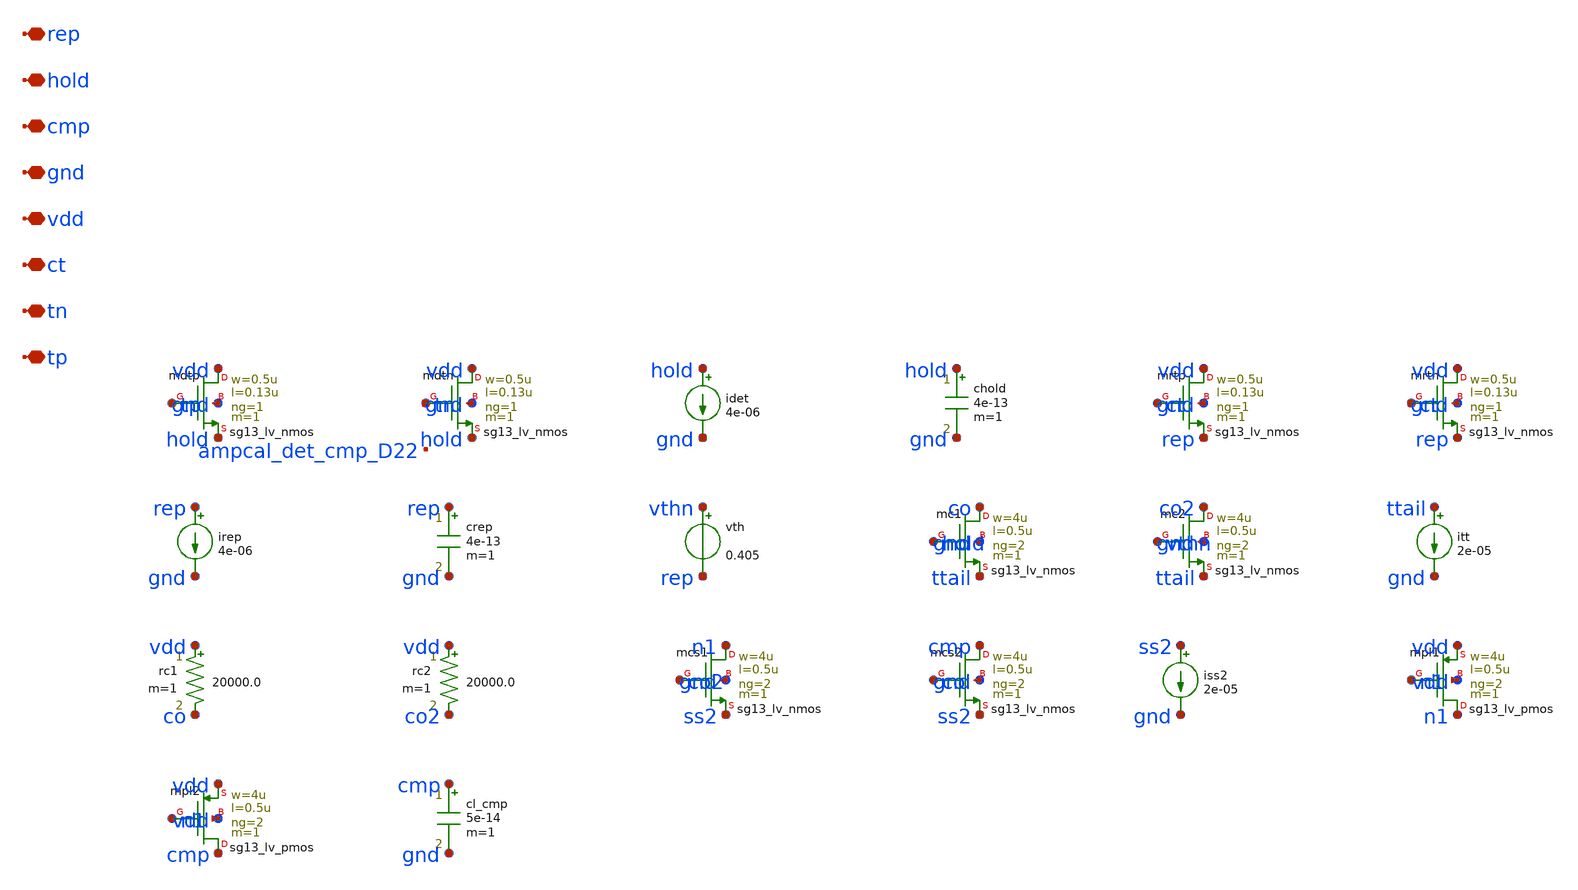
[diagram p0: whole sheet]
** sch_path: analog/vco/sch/ampcal_det.sch
**.subckt ampcal_det tp tn ct vdd gnd cmp hold rep
*.iopin tp
*.iopin tn
*.iopin ct
*.iopin vdd
*.iopin gnd
*.iopin cmp
*.iopin hold
*.iopin rep
Xmdtp vdd tp hold gnd sg13_lv_nmos w=0.5u l=0.13u ng=1 m=1 mm_ok=1
Xmdtn vdd tn hold gnd sg13_lv_nmos w=0.5u l=0.13u ng=1 m=1 mm_ok=1
idet hold gnd 4e-06
chold hold gnd 4e-13 m=1
Xmrtp vdd ct rep gnd sg13_lv_nmos w=0.5u l=0.13u ng=1 m=1 mm_ok=1
Xmrtn vdd ct rep gnd sg13_lv_nmos w=0.5u l=0.13u ng=1 m=1 mm_ok=1
irep rep gnd 4e-06
crep rep gnd 4e-13 m=1
vth vthn rep 0.405
Xmc1 co hold ttail gnd sg13_lv_nmos w=4u l=0.5u ng=2 m=1 mm_ok=1
Xmc2 co2 vthn ttail gnd sg13_lv_nmos w=4u l=0.5u ng=2 m=1 mm_ok=1
itt ttail gnd 2e-05
rc1 vdd co 20000.0 m=1
rc2 vdd co2 20000.0 m=1
Xmcs1 n1 co2 ss2 gnd sg13_lv_nmos w=4u l=0.5u ng=2 m=1 mm_ok=1
Xmcs2 cmp co ss2 gnd sg13_lv_nmos w=4u l=0.5u ng=2 m=1 mm_ok=1
iss2 ss2 gnd 2e-05
Xmpl1 n1 n1 vdd vdd sg13_lv_pmos w=4u l=0.5u ng=2 m=1 mm_ok=1
Xmpl2 cmp n1 vdd vdd sg13_lv_pmos w=4u l=0.5u ng=2 m=1 mm_ok=1
cl_cmp cmp gnd 5e-14 m=1
**.ends
.end
